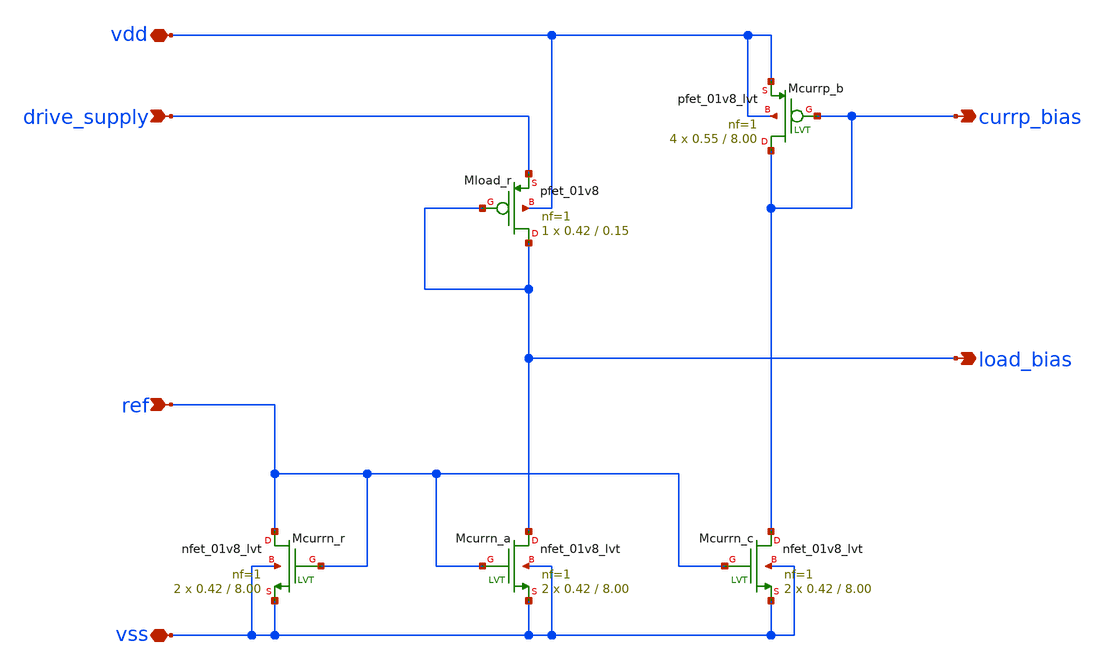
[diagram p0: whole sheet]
** sch_path: design/dac_bias/dac_bias.sch
**.subckt dac_bias vdd vss currp_bias ref load_bias drive_supply
*.iopin vdd
*.iopin vss
*.opin currp_bias
*.ipin ref
*.opin load_bias
*.ipin drive_supply
XMcurrp_b currp_bias currp_bias vdd vdd sky130_fd_pr__pfet_01v8_lvt L=8.00 W=0.55 nf=1 ad='int((nf+1)/2) * W/nf * 0.29'
+ as='int((nf+2)/2) * W/nf * 0.29' pd='2*int((nf+1)/2) * (W/nf + 0.29)' ps='2*int((nf+2)/2) * (W/nf + 0.29)'
+ nrd='0.29 / W' nrs='0.29 / W' sa=0 sb=0 sd=0 mult=4 m=4
XMcurrn_r ref ref vss vss sky130_fd_pr__nfet_01v8_lvt L=8.00 W=0.42 nf=1 ad='int((nf+1)/2) * W/nf * 0.29'
+ as='int((nf+2)/2) * W/nf * 0.29' pd='2*int((nf+1)/2) * (W/nf + 0.29)' ps='2*int((nf+2)/2) * (W/nf + 0.29)'
+ nrd='0.29 / W' nrs='0.29 / W' sa=0 sb=0 sd=0 mult=2 m=2
XMcurrn_c currp_bias ref vss vss sky130_fd_pr__nfet_01v8_lvt L=8.00 W=0.42 nf=1 ad='int((nf+1)/2) * W/nf * 0.29'
+ as='int((nf+2)/2) * W/nf * 0.29' pd='2*int((nf+1)/2) * (W/nf + 0.29)' ps='2*int((nf+2)/2) * (W/nf + 0.29)'
+ nrd='0.29 / W' nrs='0.29 / W' sa=0 sb=0 sd=0 mult=2 m=2
XMcurrn_a load_bias ref vss vss sky130_fd_pr__nfet_01v8_lvt L=8.00 W=0.42 nf=1 ad='int((nf+1)/2) * W/nf * 0.29'
+ as='int((nf+2)/2) * W/nf * 0.29' pd='2*int((nf+1)/2) * (W/nf + 0.29)' ps='2*int((nf+2)/2) * (W/nf + 0.29)'
+ nrd='0.29 / W' nrs='0.29 / W' sa=0 sb=0 sd=0 mult=2 m=2
XMload_r load_bias load_bias drive_supply vdd sky130_fd_pr__pfet_01v8 L=0.15 W=0.42 nf=1 ad='W * 0.29'
+ as='W * 0.29' pd='2 * (W + 0.29)' ps='2 * (W + 0.29)' nrd='0.29 / W' nrs='0.29 / W' sa=0 sb=0 sd=0 mult=1
+ m=1
**.ends
.end
